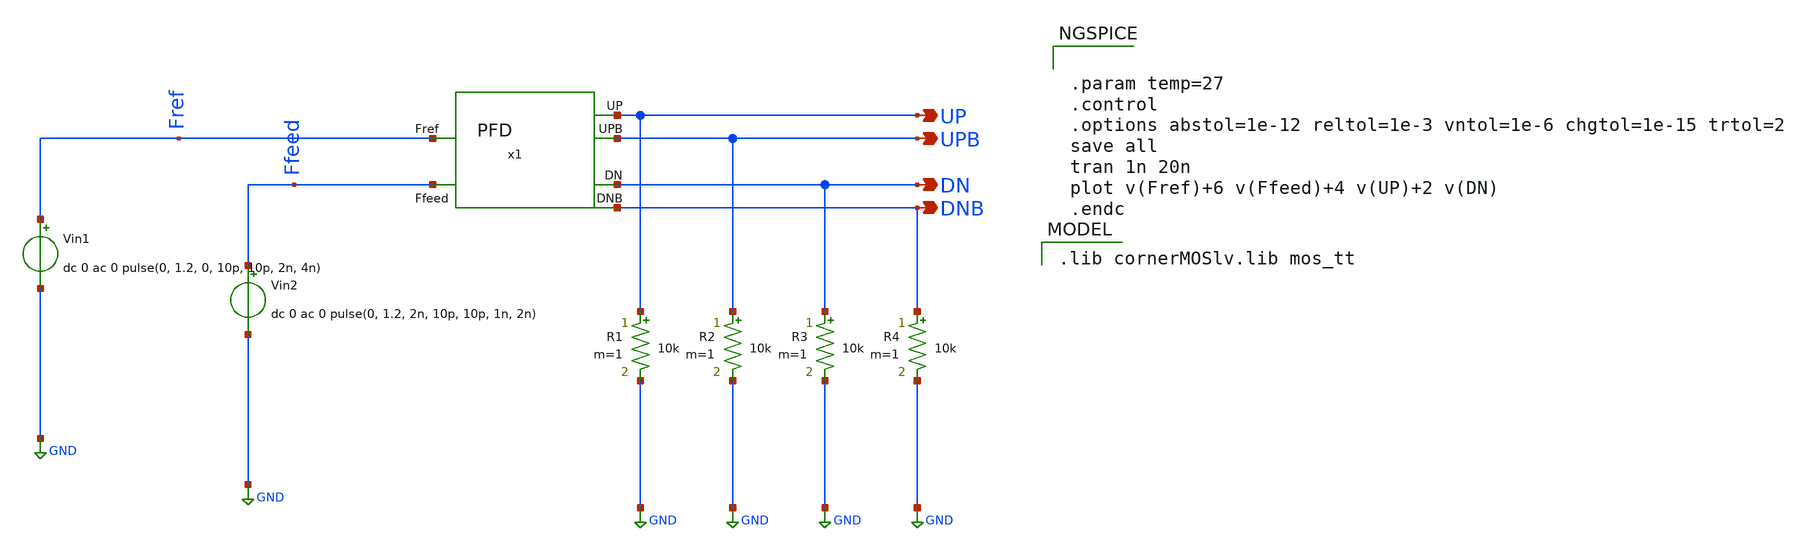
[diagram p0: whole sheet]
** sch_path: Team 1 Design/design_data/xschem/PFD/PFD_tb.sch
**.subckt PFD_tb UP UPB DN DNB
*.opin UP
*.opin UPB
*.opin DN
*.opin DNB
Vin1 Fref GND dc 0 ac 0 pulse(0, 1.2, 0, 10p, 10p, 2n, 4n)
Vin2 Ffeed GND dc 0 ac 0 pulse(0, 1.2, 2n, 10p, 10p, 1n, 2n)
x1 Fref UP UPB DN DNB Ffeed PFD
R1 UP GND 10k m=1
R2 UPB GND 10k m=1
R3 DN GND 10k m=1
R4 DNB GND 10k m=1
**** begin user architecture code
 .lib cornerMOSlv.lib mos_tt



.param temp=27
.control
.options abstol=1e-12 reltol=1e-3 vntol=1e-6 chgtol=1e-15 trtol=2
save all
tran 1n 20n
plot v(Fref)+6 v(Ffeed)+4 v(UP)+2 v(DN)
.endc


**** end user architecture code
**.ends

* expanding   symbol:  /foss/designs/Team2/PFD/PFD.sym # of pins=6
** sym_path: Team 1 Design/design_data/xschem/PFD/PFD.sym
** sch_path: Team 1 Design/design_data/xschem/PFD/PFD.sch
.subckt PFD Fref UP UPB DN DNB Ffeed
*.ipin Fref
*.ipin Ffeed
*.opin UP
*.opin UPB
*.opin DN
*.opin DNB
x3 UPB net3 net1 2NAND
x4 net2 net9 DNB 2NAND
x5 net3 net5 net4 2NAND
x6 net5 net4 net6 2NAND
x7 net6 net7 net8 2NAND
x8 net7 net8 net9 2NAND
x9 net3 net10 net5 2NAND
x10 net8 net11 net9 2NAND
x11 net10 net12 net10 2NAND
x12 net11 net13 net11 2NAND
x13 net12 net6 net13 2NAND
x14 UPB net3 net5 net6 3NAND
x15 DNB net6 net8 net9 3NAND
x1 Fref net1 Fref 2NAND
x2 Ffeed net2 Ffeed 2NAND
x16 UPB UP UPB 2NAND
x17 DNB DN DNB 2NAND
.ends


* expanding   symbol:  /foss/designs/Team2/2NAND/2NAND.sym # of pins=3
** sym_path: Team 1 Design/design_data/xschem/2_Input_NAND/2NAND.sym
** sch_path: Team 1 Design/design_data/xschem/2_Input_NAND/2NAND.sch
.subckt 2NAND A Y B
*.ipin B
*.opin Y
*.ipin A
XM1 Y A net1 net1 sg13_lv_pmos w=2u l=0.13u ng=1 m=1 mm_ok=1
XM2 Y B net1 net1 sg13_lv_pmos w=2u l=0.13u ng=1 m=1 mm_ok=1
XM3 Y B net2 GND sg13_lv_nmos w=1u l=0.13u ng=1 m=1 mm_ok=1
XM4 net2 A GND GND sg13_lv_nmos w=1u l=0.13u ng=1 m=1 mm_ok=1
V1 net1 GND 1.2
.ends


* expanding   symbol:  /foss/designs/Team2/3NAND/3NAND.sym # of pins=4
** sym_path: Team 1 Design/design_data/xschem/3_Input_NAND/3NAND.sym
** sch_path: Team 1 Design/design_data/xschem/3_Input_NAND/3NAND.sch
.subckt 3NAND Y A B C
*.ipin A
*.ipin B
*.ipin C
*.opin Y
XM1 Y A Vdd Vdd sg13_lv_pmos w=2u l=0.13u ng=1 m=1 mm_ok=1
XM2 Y B Vdd Vdd sg13_lv_pmos w=2u l=0.13u ng=1 m=1 mm_ok=1
XM3 Y C Vdd Vdd sg13_lv_pmos w=2u l=0.13u ng=1 m=1 mm_ok=1
XM4 Y A net1 GND sg13_lv_nmos w=1u l=0.13u ng=1 m=1 mm_ok=1
XM5 net1 B net2 GND sg13_lv_nmos w=1u l=0.13u ng=1 m=1 mm_ok=1
XM6 net2 C GND GND sg13_lv_nmos w=1u l=0.13u ng=1 m=1 mm_ok=1
V1 Vdd GND 1.2
.ends

.GLOBAL GND
.end
